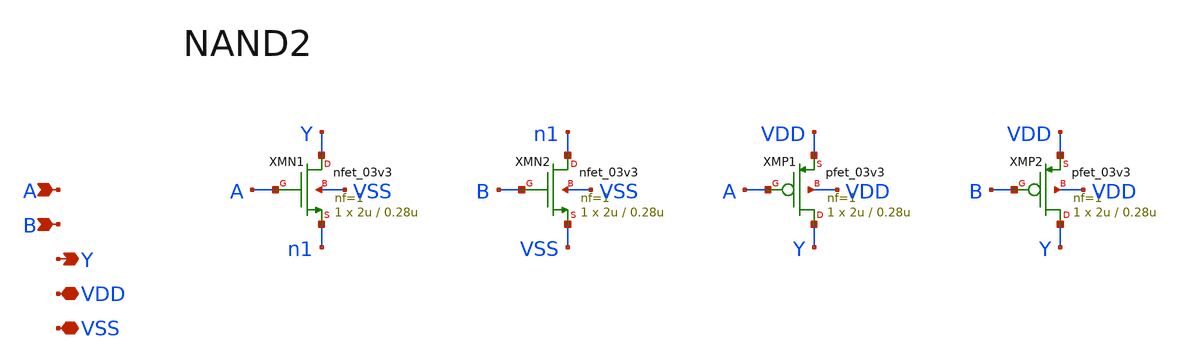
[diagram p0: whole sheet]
** sch_path: v1_claude/xschem/nand2.sch
**.subckt nand2 A B Y VDD VSS
*.ipin A
*.ipin B
*.opin Y
*.iopin VDD
*.iopin VSS
XMN1 Y A n1 VSS nfet_03v3 L=0.28u W=2u nf=1 ad='int((nf+1)/2) * W/nf * 0.18u' as='int((nf+2)/2) * W/nf * 0.18u'
+ pd='2*int((nf+1)/2) * (W/nf + 0.18u)' ps='2*int((nf+2)/2) * (W/nf + 0.18u)' nrd='0.18u / W' nrs='0.18u / W'
+ sa=0 sb=0 sd=0 m=1
XMN2 n1 B VSS VSS nfet_03v3 L=0.28u W=2u nf=1 ad='int((nf+1)/2) * W/nf * 0.18u' as='int((nf+2)/2) * W/nf * 0.18u'
+ pd='2*int((nf+1)/2) * (W/nf + 0.18u)' ps='2*int((nf+2)/2) * (W/nf + 0.18u)' nrd='0.18u / W' nrs='0.18u / W'
+ sa=0 sb=0 sd=0 m=1
XMP1 Y A VDD VDD pfet_03v3 L=0.28u W=2u nf=1 ad='int((nf+1)/2) * W/nf * 0.18u' as='int((nf+2)/2) * W/nf * 0.18u'
+ pd='2*int((nf+1)/2) * (W/nf + 0.18u)' ps='2*int((nf+2)/2) * (W/nf + 0.18u)' nrd='0.18u / W' nrs='0.18u / W'
+ sa=0 sb=0 sd=0 m=1
XMP2 Y B VDD VDD pfet_03v3 L=0.28u W=2u nf=1 ad='int((nf+1)/2) * W/nf * 0.18u' as='int((nf+2)/2) * W/nf * 0.18u'
+ pd='2*int((nf+1)/2) * (W/nf + 0.18u)' ps='2*int((nf+2)/2) * (W/nf + 0.18u)' nrd='0.18u / W' nrs='0.18u / W'
+ sa=0 sb=0 sd=0 m=1
**.ends
.end
